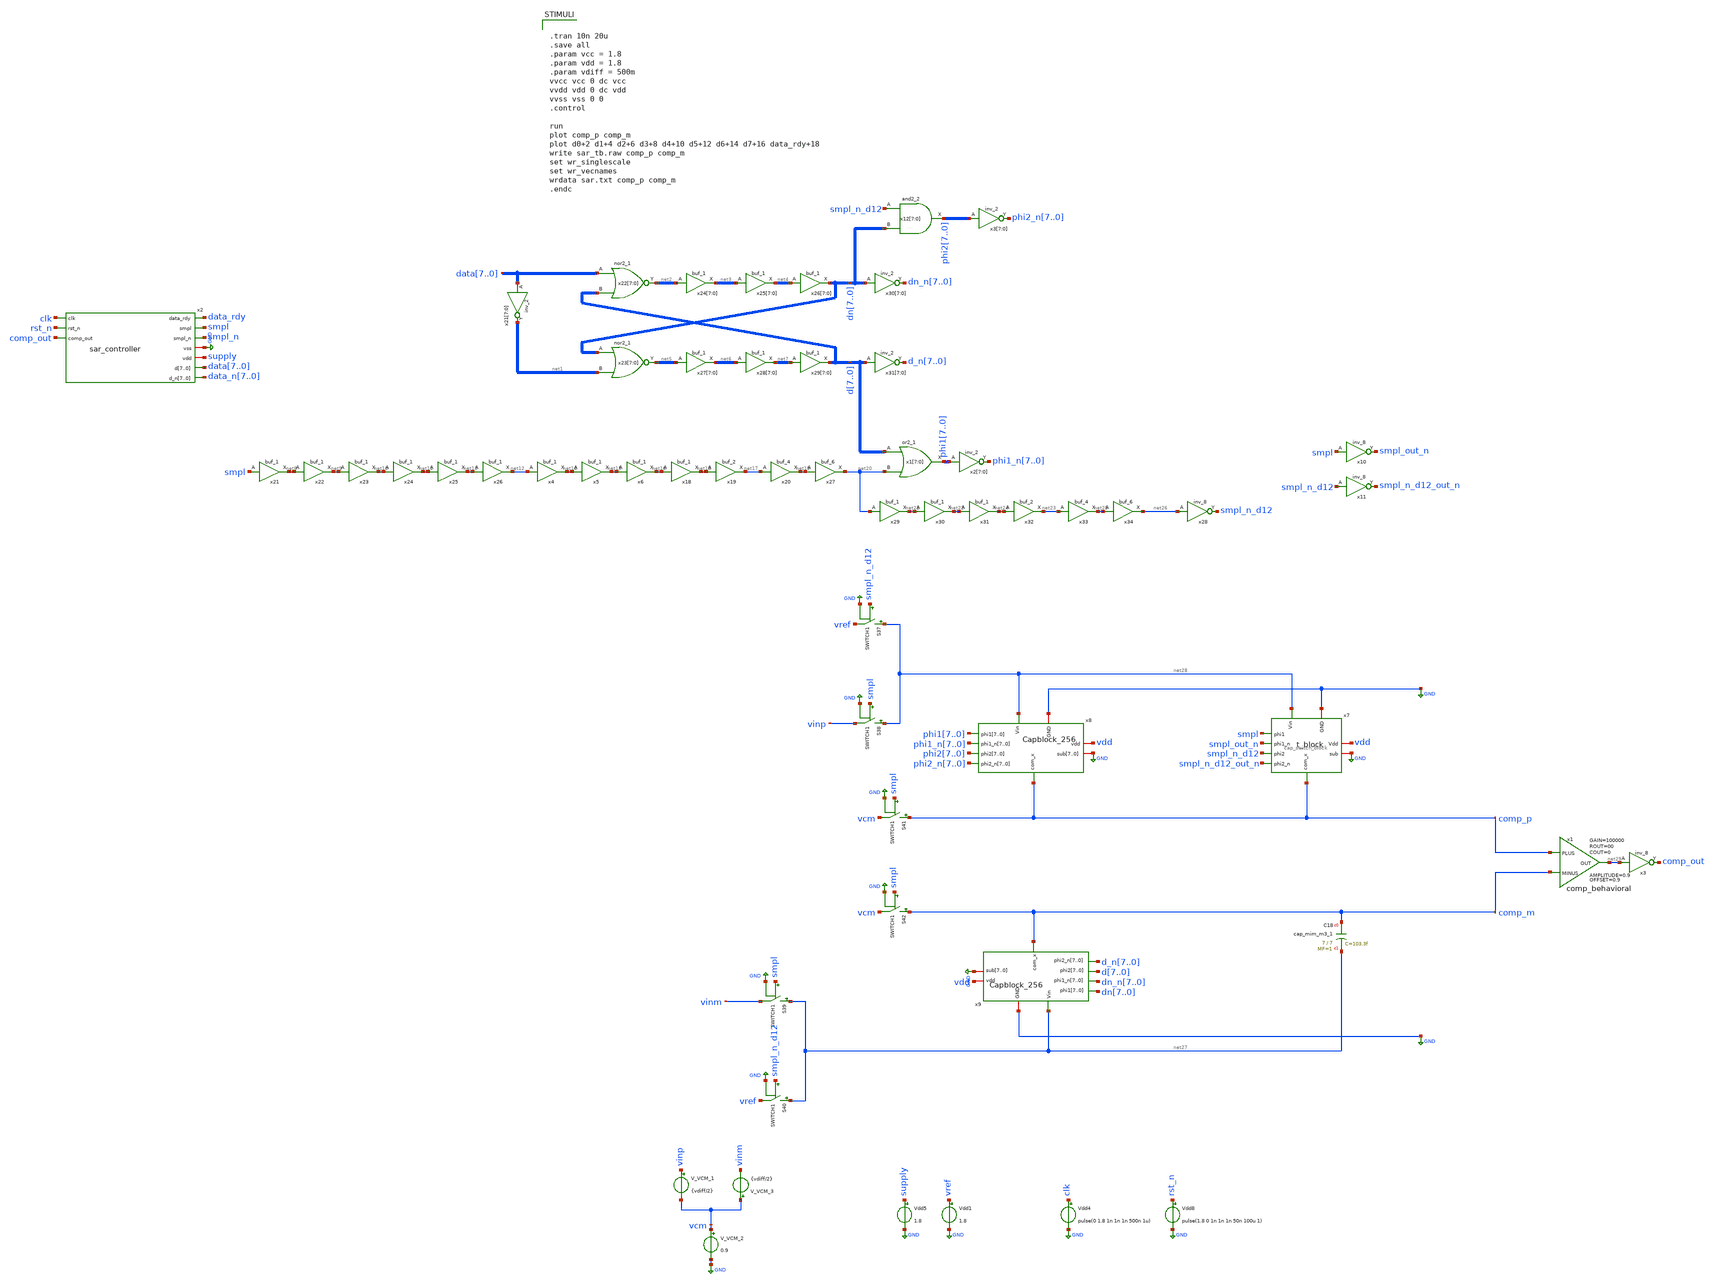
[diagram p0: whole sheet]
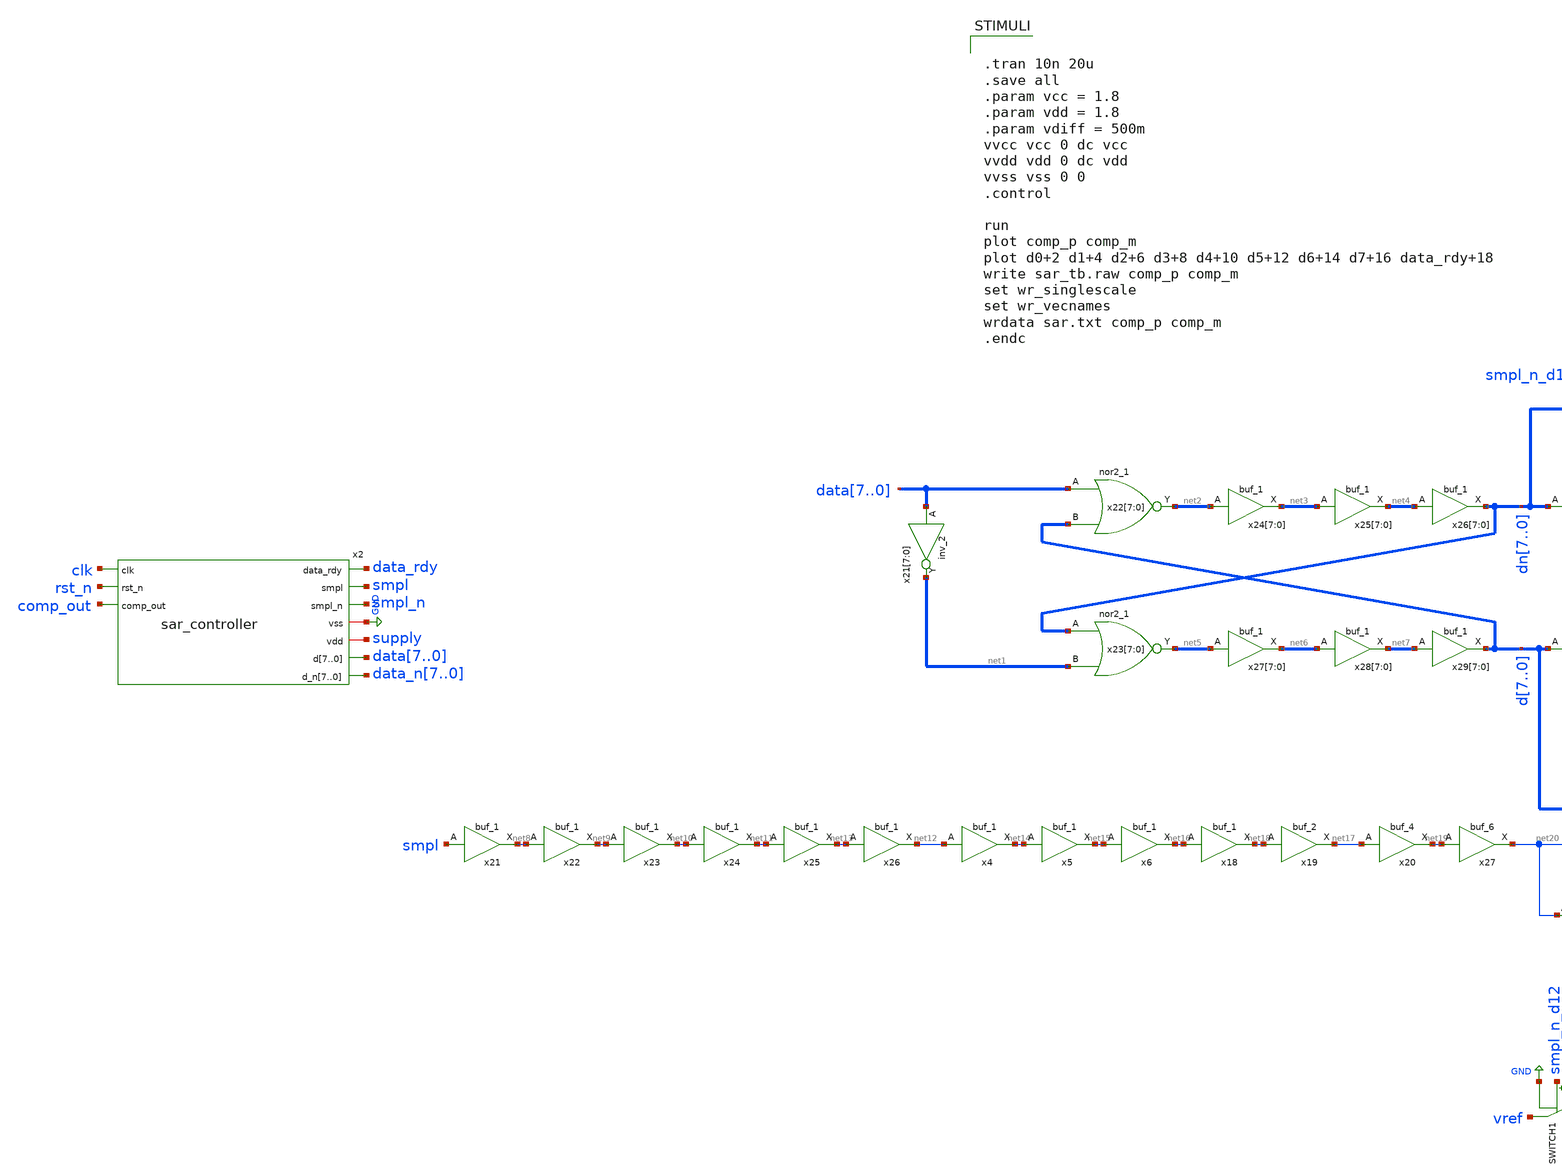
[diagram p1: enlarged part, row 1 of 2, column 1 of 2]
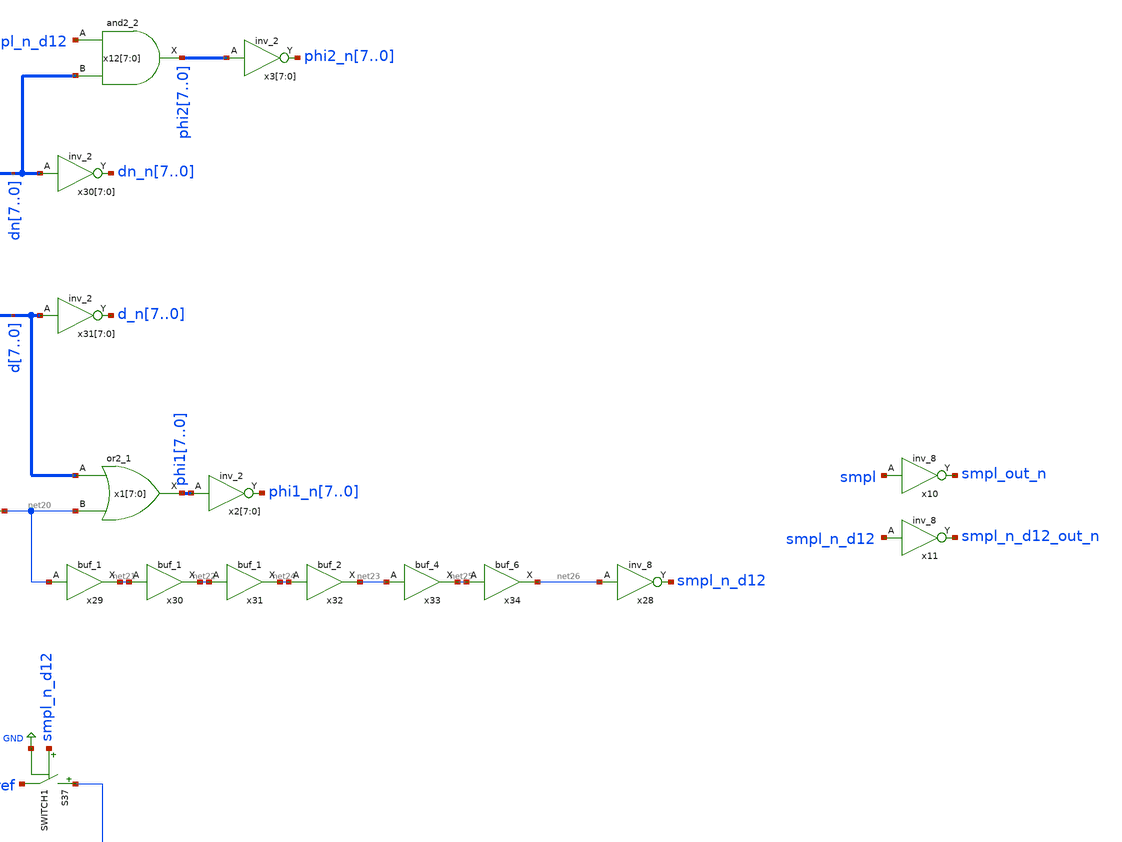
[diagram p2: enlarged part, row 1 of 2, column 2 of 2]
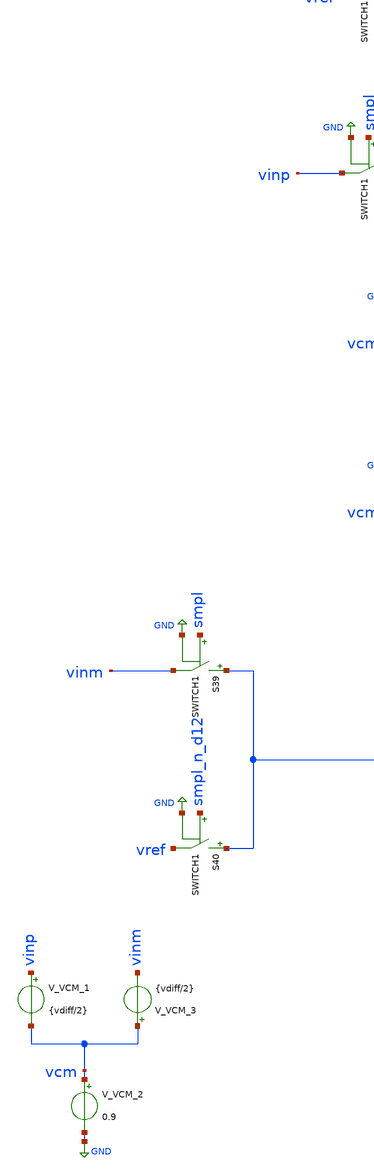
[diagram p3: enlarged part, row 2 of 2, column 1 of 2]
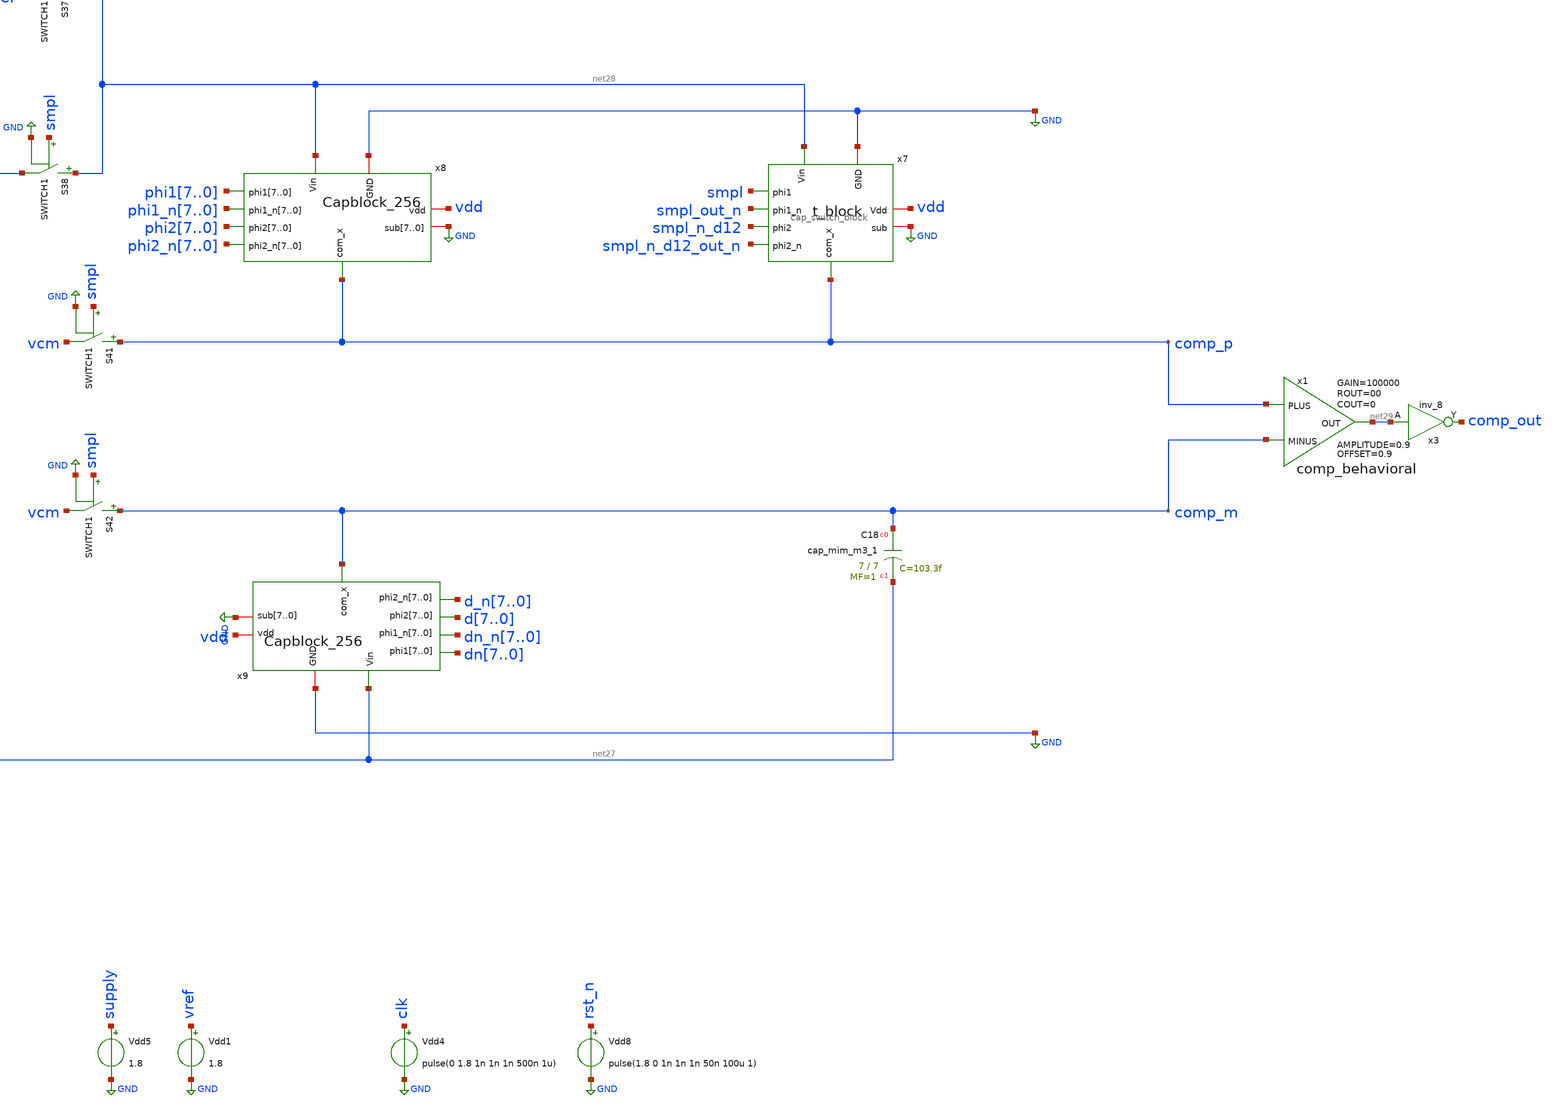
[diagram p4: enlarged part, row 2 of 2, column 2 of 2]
** sch_path: test/testbench/sar_tb_replace_cblock256.sch
.lib $::SKYWATER_MODELS/sky130.lib.spice tt
.include $::SKYWATER_STDCELLS/sky130_fd_sc_hd.spice

**.subckt sar_tb_replace_cblock256
Vdd8 rst_n GND pulse(1.8 0 1n 1n 1n 50n 100u 1)
Vdd4 clk GND pulse(0 1.8 1n 1n 1n 500n 1u)
Vdd1 vref GND 1.8
Vdd5 supply GND 1.8
V_VCM_2 vcm GND 0.9
V_VCM_1 vinp vcm {vdiff/2}
V_VCM_3 vcm vinm {vdiff/2}
x21[7] data7 vss vss vcc vcc net1[7] sky130_fd_sc_hd__inv_2
x21[6] data6 vss vss vcc vcc net1[6] sky130_fd_sc_hd__inv_2
x21[5] data5 vss vss vcc vcc net1[5] sky130_fd_sc_hd__inv_2
x21[4] data4 vss vss vcc vcc net1[4] sky130_fd_sc_hd__inv_2
x21[3] data3 vss vss vcc vcc net1[3] sky130_fd_sc_hd__inv_2
x21[2] data2 vss vss vcc vcc net1[2] sky130_fd_sc_hd__inv_2
x21[1] data1 vss vss vcc vcc net1[1] sky130_fd_sc_hd__inv_2
x21[0] data0 vss vss vcc vcc net1[0] sky130_fd_sc_hd__inv_2
x22[7] data7 d7 vss vss vdd vdd net2[7] sky130_fd_sc_hd__nor2_1
x22[6] data6 d6 vss vss vdd vdd net2[6] sky130_fd_sc_hd__nor2_1
x22[5] data5 d5 vss vss vdd vdd net2[5] sky130_fd_sc_hd__nor2_1
x22[4] data4 d4 vss vss vdd vdd net2[4] sky130_fd_sc_hd__nor2_1
x22[3] data3 d3 vss vss vdd vdd net2[3] sky130_fd_sc_hd__nor2_1
x22[2] data2 d2 vss vss vdd vdd net2[2] sky130_fd_sc_hd__nor2_1
x22[1] data1 d1 vss vss vdd vdd net2[1] sky130_fd_sc_hd__nor2_1
x22[0] data0 d0 vss vss vdd vdd net2[0] sky130_fd_sc_hd__nor2_1
x23[7] dn7 net1[7] vss vss vdd vdd net5[7] sky130_fd_sc_hd__nor2_1
x23[6] dn6 net1[6] vss vss vdd vdd net5[6] sky130_fd_sc_hd__nor2_1
x23[5] dn5 net1[5] vss vss vdd vdd net5[5] sky130_fd_sc_hd__nor2_1
x23[4] dn4 net1[4] vss vss vdd vdd net5[4] sky130_fd_sc_hd__nor2_1
x23[3] dn3 net1[3] vss vss vdd vdd net5[3] sky130_fd_sc_hd__nor2_1
x23[2] dn2 net1[2] vss vss vdd vdd net5[2] sky130_fd_sc_hd__nor2_1
x23[1] dn1 net1[1] vss vss vdd vdd net5[1] sky130_fd_sc_hd__nor2_1
x23[0] dn0 net1[0] vss vss vdd vdd net5[0] sky130_fd_sc_hd__nor2_1
x24[7] net2[7] vss vss vdd vdd net3[7] sky130_fd_sc_hd__buf_1
x24[6] net2[6] vss vss vdd vdd net3[6] sky130_fd_sc_hd__buf_1
x24[5] net2[5] vss vss vdd vdd net3[5] sky130_fd_sc_hd__buf_1
x24[4] net2[4] vss vss vdd vdd net3[4] sky130_fd_sc_hd__buf_1
x24[3] net2[3] vss vss vdd vdd net3[3] sky130_fd_sc_hd__buf_1
x24[2] net2[2] vss vss vdd vdd net3[2] sky130_fd_sc_hd__buf_1
x24[1] net2[1] vss vss vdd vdd net3[1] sky130_fd_sc_hd__buf_1
x24[0] net2[0] vss vss vdd vdd net3[0] sky130_fd_sc_hd__buf_1
x25[7] net3[7] vss vss vdd vdd net4[7] sky130_fd_sc_hd__buf_1
x25[6] net3[6] vss vss vdd vdd net4[6] sky130_fd_sc_hd__buf_1
x25[5] net3[5] vss vss vdd vdd net4[5] sky130_fd_sc_hd__buf_1
x25[4] net3[4] vss vss vdd vdd net4[4] sky130_fd_sc_hd__buf_1
x25[3] net3[3] vss vss vdd vdd net4[3] sky130_fd_sc_hd__buf_1
x25[2] net3[2] vss vss vdd vdd net4[2] sky130_fd_sc_hd__buf_1
x25[1] net3[1] vss vss vdd vdd net4[1] sky130_fd_sc_hd__buf_1
x25[0] net3[0] vss vss vdd vdd net4[0] sky130_fd_sc_hd__buf_1
x26[7] net4[7] vss vss vdd vdd dn7 sky130_fd_sc_hd__buf_1
x26[6] net4[6] vss vss vdd vdd dn6 sky130_fd_sc_hd__buf_1
x26[5] net4[5] vss vss vdd vdd dn5 sky130_fd_sc_hd__buf_1
x26[4] net4[4] vss vss vdd vdd dn4 sky130_fd_sc_hd__buf_1
x26[3] net4[3] vss vss vdd vdd dn3 sky130_fd_sc_hd__buf_1
x26[2] net4[2] vss vss vdd vdd dn2 sky130_fd_sc_hd__buf_1
x26[1] net4[1] vss vss vdd vdd dn1 sky130_fd_sc_hd__buf_1
x26[0] net4[0] vss vss vdd vdd dn0 sky130_fd_sc_hd__buf_1
x27[7] net5[7] vss vss vdd vdd net6[7] sky130_fd_sc_hd__buf_1
x27[6] net5[6] vss vss vdd vdd net6[6] sky130_fd_sc_hd__buf_1
x27[5] net5[5] vss vss vdd vdd net6[5] sky130_fd_sc_hd__buf_1
x27[4] net5[4] vss vss vdd vdd net6[4] sky130_fd_sc_hd__buf_1
x27[3] net5[3] vss vss vdd vdd net6[3] sky130_fd_sc_hd__buf_1
x27[2] net5[2] vss vss vdd vdd net6[2] sky130_fd_sc_hd__buf_1
x27[1] net5[1] vss vss vdd vdd net6[1] sky130_fd_sc_hd__buf_1
x27[0] net5[0] vss vss vdd vdd net6[0] sky130_fd_sc_hd__buf_1
x28[7] net6[7] vss vss vdd vdd net7[7] sky130_fd_sc_hd__buf_1
x28[6] net6[6] vss vss vdd vdd net7[6] sky130_fd_sc_hd__buf_1
x28[5] net6[5] vss vss vdd vdd net7[5] sky130_fd_sc_hd__buf_1
x28[4] net6[4] vss vss vdd vdd net7[4] sky130_fd_sc_hd__buf_1
x28[3] net6[3] vss vss vdd vdd net7[3] sky130_fd_sc_hd__buf_1
x28[2] net6[2] vss vss vdd vdd net7[2] sky130_fd_sc_hd__buf_1
x28[1] net6[1] vss vss vdd vdd net7[1] sky130_fd_sc_hd__buf_1
x28[0] net6[0] vss vss vdd vdd net7[0] sky130_fd_sc_hd__buf_1
x29[7] net7[7] vss vss vdd vdd d7 sky130_fd_sc_hd__buf_1
x29[6] net7[6] vss vss vdd vdd d6 sky130_fd_sc_hd__buf_1
x29[5] net7[5] vss vss vdd vdd d5 sky130_fd_sc_hd__buf_1
x29[4] net7[4] vss vss vdd vdd d4 sky130_fd_sc_hd__buf_1
x29[3] net7[3] vss vss vdd vdd d3 sky130_fd_sc_hd__buf_1
x29[2] net7[2] vss vss vdd vdd d2 sky130_fd_sc_hd__buf_1
x29[1] net7[1] vss vss vdd vdd d1 sky130_fd_sc_hd__buf_1
x29[0] net7[0] vss vss vdd vdd d0 sky130_fd_sc_hd__buf_1
x30[7] dn7 vss vss vcc vcc dn_n7 sky130_fd_sc_hd__inv_2
x30[6] dn6 vss vss vcc vcc dn_n6 sky130_fd_sc_hd__inv_2
x30[5] dn5 vss vss vcc vcc dn_n5 sky130_fd_sc_hd__inv_2
x30[4] dn4 vss vss vcc vcc dn_n4 sky130_fd_sc_hd__inv_2
x30[3] dn3 vss vss vcc vcc dn_n3 sky130_fd_sc_hd__inv_2
x30[2] dn2 vss vss vcc vcc dn_n2 sky130_fd_sc_hd__inv_2
x30[1] dn1 vss vss vcc vcc dn_n1 sky130_fd_sc_hd__inv_2
x30[0] dn0 vss vss vcc vcc dn_n0 sky130_fd_sc_hd__inv_2
x31[7] d7 vss vss vcc vcc d_n7 sky130_fd_sc_hd__inv_2
x31[6] d6 vss vss vcc vcc d_n6 sky130_fd_sc_hd__inv_2
x31[5] d5 vss vss vcc vcc d_n5 sky130_fd_sc_hd__inv_2
x31[4] d4 vss vss vcc vcc d_n4 sky130_fd_sc_hd__inv_2
x31[3] d3 vss vss vcc vcc d_n3 sky130_fd_sc_hd__inv_2
x31[2] d2 vss vss vcc vcc d_n2 sky130_fd_sc_hd__inv_2
x31[1] d1 vss vss vcc vcc d_n1 sky130_fd_sc_hd__inv_2
x31[0] d0 vss vss vcc vcc d_n0 sky130_fd_sc_hd__inv_2
x1[7] d7 net20 vss vss vcc vcc phi17 sky130_fd_sc_hd__or2_1
x1[6] d6 net20 vss vss vcc vcc phi16 sky130_fd_sc_hd__or2_1
x1[5] d5 net20 vss vss vcc vcc phi15 sky130_fd_sc_hd__or2_1
x1[4] d4 net20 vss vss vcc vcc phi14 sky130_fd_sc_hd__or2_1
x1[3] d3 net20 vss vss vcc vcc phi13 sky130_fd_sc_hd__or2_1
x1[2] d2 net20 vss vss vcc vcc phi12 sky130_fd_sc_hd__or2_1
x1[1] d1 net20 vss vss vcc vcc phi11 sky130_fd_sc_hd__or2_1
x1[0] d0 net20 vss vss vcc vcc phi10 sky130_fd_sc_hd__or2_1
x21 smpl vss vss vdd vdd net8 sky130_fd_sc_hd__buf_1
x22 net8 vss vss vdd vdd net9 sky130_fd_sc_hd__buf_1
x23 net9 vss vss vdd vdd net10 sky130_fd_sc_hd__buf_1
x24 net10 vss vss vdd vdd net11 sky130_fd_sc_hd__buf_1
x25 net11 vss vss vdd vdd net13 sky130_fd_sc_hd__buf_1
x26 net13 vss vss vdd vdd net12 sky130_fd_sc_hd__buf_1
x2[7] phi17 vss vss vcc vcc phi1_n7 sky130_fd_sc_hd__inv_2
x2[6] phi16 vss vss vcc vcc phi1_n6 sky130_fd_sc_hd__inv_2
x2[5] phi15 vss vss vcc vcc phi1_n5 sky130_fd_sc_hd__inv_2
x2[4] phi14 vss vss vcc vcc phi1_n4 sky130_fd_sc_hd__inv_2
x2[3] phi13 vss vss vcc vcc phi1_n3 sky130_fd_sc_hd__inv_2
x2[2] phi12 vss vss vcc vcc phi1_n2 sky130_fd_sc_hd__inv_2
x2[1] phi11 vss vss vcc vcc phi1_n1 sky130_fd_sc_hd__inv_2
x2[0] phi10 vss vss vcc vcc phi1_n0 sky130_fd_sc_hd__inv_2
x12[7] smpl_n_d12 dn7 vss vss vcc vcc phi27 sky130_fd_sc_hd__and2_2
x12[6] smpl_n_d12 dn6 vss vss vcc vcc phi26 sky130_fd_sc_hd__and2_2
x12[5] smpl_n_d12 dn5 vss vss vcc vcc phi25 sky130_fd_sc_hd__and2_2
x12[4] smpl_n_d12 dn4 vss vss vcc vcc phi24 sky130_fd_sc_hd__and2_2
x12[3] smpl_n_d12 dn3 vss vss vcc vcc phi23 sky130_fd_sc_hd__and2_2
x12[2] smpl_n_d12 dn2 vss vss vcc vcc phi22 sky130_fd_sc_hd__and2_2
x12[1] smpl_n_d12 dn1 vss vss vcc vcc phi21 sky130_fd_sc_hd__and2_2
x12[0] smpl_n_d12 dn0 vss vss vcc vcc phi20 sky130_fd_sc_hd__and2_2
x4 net12 vss vss vdd vdd net14 sky130_fd_sc_hd__buf_1
x5 net14 vss vss vdd vdd net15 sky130_fd_sc_hd__buf_1
x6 net15 vss vss vdd vdd net16 sky130_fd_sc_hd__buf_1
x18 net16 vss vss vdd vdd net18 sky130_fd_sc_hd__buf_1
x19 net18 vss vss vdd vdd net17 sky130_fd_sc_hd__buf_2
x20 net17 vss vss vdd vdd net19 sky130_fd_sc_hd__buf_4
x27 net19 vss vss vdd vdd net20 sky130_fd_sc_hd__buf_6
x28 net26 vss vss vcc vcc smpl_n_d12 sky130_fd_sc_hd__inv_8
x29 net20 vss vss vdd vdd net21 sky130_fd_sc_hd__buf_1
x30 net21 vss vss vdd vdd net22 sky130_fd_sc_hd__buf_1
x31 net22 vss vss vdd vdd net24 sky130_fd_sc_hd__buf_1
x32 net24 vss vss vdd vdd net23 sky130_fd_sc_hd__buf_2
x33 net23 vss vss vdd vdd net25 sky130_fd_sc_hd__buf_4
x34 net25 vss vss vdd vdd net26 sky130_fd_sc_hd__buf_6
x3[7] phi27 vss vss vcc vcc phi2_n7 sky130_fd_sc_hd__inv_2
x3[6] phi26 vss vss vcc vcc phi2_n6 sky130_fd_sc_hd__inv_2
x3[5] phi25 vss vss vcc vcc phi2_n5 sky130_fd_sc_hd__inv_2
x3[4] phi24 vss vss vcc vcc phi2_n4 sky130_fd_sc_hd__inv_2
x3[3] phi23 vss vss vcc vcc phi2_n3 sky130_fd_sc_hd__inv_2
x3[2] phi22 vss vss vcc vcc phi2_n2 sky130_fd_sc_hd__inv_2
x3[1] phi21 vss vss vcc vcc phi2_n1 sky130_fd_sc_hd__inv_2
x3[0] phi20 vss vss vcc vcc phi2_n0 sky130_fd_sc_hd__inv_2
x2 clk data_rdy smpl rst_n smpl_n comp_out GND supply data7 data6 data5 data4 data3 data2 data1
+ data0 data_n7 data_n6 data_n5 data_n4 data_n3 data_n2 data_n1 data_n0 sar_controller
XC18 comp_m net27 sky130_fd_pr__cap_mim_m3_1 W=7 L=7 MF=1 m=1
S37 net28 vref smpl_n_d12 GND SWITCH1
S41 comp_p vcm smpl GND SWITCH1
S42 comp_m vcm smpl GND SWITCH1
S38 net28 vinp smpl GND SWITCH1
x3 net29 vss vss vcc vcc comp_out sky130_fd_sc_hd__inv_8
x7 net28 GND GND vdd smpl smpl_n_d12 smpl_n_d12_out_n smpl_out_n comp_p cap_switch_block
x1 comp_p comp_m net29 comp_behavioral OFFSET=0.9 AMPLITUDE=0.9 GAIN=100000 ROUT=00 COUT=0
x8 GND phi17 phi16 phi15 phi14 phi13 phi12 phi11 phi10 phi1_n7 phi1_n6 phi1_n5 phi1_n4 phi1_n3
+ phi1_n2 phi1_n1 phi1_n0 phi27 phi26 phi25 phi24 phi23 phi22 phi21 phi20 phi2_n7 phi2_n6 phi2_n5 phi2_n4
+ phi2_n3 phi2_n2 phi2_n1 phi2_n0 comp_p net28 GND GND GND GND GND GND GND GND vdd capblock_256
x9 GND dn7 dn6 dn5 dn4 dn3 dn2 dn1 dn0 dn_n7 dn_n6 dn_n5 dn_n4 dn_n3 dn_n2 dn_n1 dn_n0 d7 d6 d5 d4
+ d3 d2 d1 d0 d_n7 d_n6 d_n5 d_n4 d_n3 d_n2 d_n1 d_n0 comp_m net27 GND GND GND GND GND GND GND GND vdd
+ capblock_256
S39 net27 vinm smpl GND SWITCH1
S40 net27 vref smpl_n_d12 GND SWITCH1
x10 smpl vss vss vcc vcc smpl_out_n sky130_fd_sc_hd__inv_8
x11 smpl_n_d12 vss vss vcc vcc smpl_n_d12_out_n sky130_fd_sc_hd__inv_8
**** begin user architecture code


.tran 10n 20u
.save all
.param vcc = 1.8
.param vdd = 1.8
.param vdiff = 500m
vvcc vcc 0 dc vcc
vvdd vdd 0 dc vdd
vvss vss 0 0
.control

run
plot comp_p comp_m
plot d0+2 d1+4 d2+6 d3+8 d4+10 d5+12 d6+14 d7+16 data_rdy+18
write sar_tb.raw comp_p comp_m
set wr_singlescale
set wr_vecnames
wrdata sar.txt comp_p comp_m
.endc



.model SWITCH1 sw vt=0.9 vh=0 ron=1 roff =100G

**** end user architecture code
**.ends

* expanding   symbol:  sar_controller.sym # of pins=10
** sym_path: test/design/sar_controller.sym
** sch_path: test/design/sar_controller.sch
.subckt sar_controller clk data_rdy smpl rst_n smpl_n comp_out vss vdd d7 d6 d5 d4 d3 d2 d1 d0 d_n7
+ d_n6 d_n5 d_n4 d_n3 d_n2 d_n1 d_n0
*.ipin rst_n
*.opin data_rdy
*.ipin clk
*.opin smpl
*.ipin comp_out
*.iopin vss
*.iopin vdd
*.opin d7,d6,d5,d4,d3,d2,d1,d0
*.opin d_n7,d_n6,d_n5,d_n4,d_n3,d_n2,d_n1,d_n0
*.opin smpl_n
x26 net2 net21 net22 net9 vss vss vdd vdd net1 net25 sky130_fd_sc_hd__dfbbp_1
x5 net19 net23 net20 vss vss vdd vdd cnv_7 net9 sky130_fd_sc_hd__dfrbp_1
* noconn #net33
x24 net19 net8 net20 vss vss vdd vdd net23 net24 sky130_fd_sc_hd__dfsbp_1
x6 net24 net20 vss vss vdd vdd net22 sky130_fd_sc_hd__and2_4
x1 net19 cnv_7 net20 vss vss vdd vdd cnv_6 net12 sky130_fd_sc_hd__dfrbp_1
x2 net19 cnv_6 net20 vss vss vdd vdd cnv_5 net13 sky130_fd_sc_hd__dfrbp_1
x3 net19 cnv_5 net20 vss vss vdd vdd cnv_4 net14 sky130_fd_sc_hd__dfrbp_1
x4 net19 cnv_4 net20 vss vss vdd vdd cnv_3 net15 sky130_fd_sc_hd__dfrbp_1
x7 net19 cnv_3 net20 vss vss vdd vdd cnv_2 net16 sky130_fd_sc_hd__dfrbp_1
x8 net19 cnv_2 net20 vss vss vdd vdd cnv_1 net17 sky130_fd_sc_hd__dfrbp_1
x9 net19 cnv_1 net20 vss vss vdd vdd cnv_0 net18 sky130_fd_sc_hd__dfrbp_1
x10 net19 cnv_0 net20 vss vss vdd vdd net8 net33 sky130_fd_sc_hd__dfrbp_1
x11 vss vss net22 vss vss vdd vdd net11 net34 sky130_fd_sc_hd__dfrbp_1
x12 net10 net21 net22 net12 vss vss vdd vdd net2 net26 sky130_fd_sc_hd__dfbbp_1
x13 net3 net21 net22 net13 vss vss vdd vdd net10 net27 sky130_fd_sc_hd__dfbbp_1
x14 net4 net21 net22 net14 vss vss vdd vdd net3 net28 sky130_fd_sc_hd__dfbbp_1
x15 net5 net21 net22 net15 vss vss vdd vdd net4 net29 sky130_fd_sc_hd__dfbbp_1
x16 net6 net21 net22 net16 vss vss vdd vdd net5 net30 sky130_fd_sc_hd__dfbbp_1
x17 net7 net21 net22 net17 vss vss vdd vdd net6 net31 sky130_fd_sc_hd__dfbbp_1
x18 net11 net21 net22 net18 vss vss vdd vdd net7 net32 sky130_fd_sc_hd__dfbbp_1
* noconn #net34
x19 net1 vss vss vdd vdd d7 sky130_fd_sc_hd__buf_2
x20 net25 vss vss vdd vdd d_n7 sky130_fd_sc_hd__buf_2
x21 net2 vss vss vdd vdd d6 sky130_fd_sc_hd__buf_2
x22 net26 vss vss vdd vdd d_n6 sky130_fd_sc_hd__buf_2
x23 net10 vss vss vdd vdd d5 sky130_fd_sc_hd__buf_2
x25 net27 vss vss vdd vdd d_n5 sky130_fd_sc_hd__buf_2
x27 net3 vss vss vdd vdd d4 sky130_fd_sc_hd__buf_2
x28 net28 vss vss vdd vdd d_n4 sky130_fd_sc_hd__buf_2
x29 net4 vss vss vdd vdd d3 sky130_fd_sc_hd__buf_2
x30 net29 vss vss vdd vdd d_n3 sky130_fd_sc_hd__buf_2
x31 net5 vss vss vdd vdd d2 sky130_fd_sc_hd__buf_2
x32 net30 vss vss vdd vdd d_n2 sky130_fd_sc_hd__buf_2
x33 net6 vss vss vdd vdd d1 sky130_fd_sc_hd__buf_2
x34 net31 vss vss vdd vdd d_n1 sky130_fd_sc_hd__buf_2
x35 net7 vss vss vdd vdd d0 sky130_fd_sc_hd__buf_2
x36 net32 vss vss vdd vdd d_n0 sky130_fd_sc_hd__buf_2
x37 net23 vss vss vdd vdd smpl sky130_fd_sc_hd__buf_2
x38 net24 vss vss vdd vdd smpl_n sky130_fd_sc_hd__buf_2
x39 net8 vss vss vdd vdd data_rdy sky130_fd_sc_hd__buf_2
x40 comp_out vss vss vdd vdd net21 sky130_fd_sc_hd__buf_4
x41 rst_n vss vss vdd vdd net20 sky130_fd_sc_hd__buf_4
x42 clk vss vss vdd vdd net19 sky130_fd_sc_hd__buf_4
.ends


* expanding   symbol:  cap_switch_block.sym # of pins=9
** sym_path: test/design/cap_switch_block.sym
** sch_path: test/design/cap_switch_block.sch
.subckt cap_switch_block Vin sub GND Vdd phi1 phi2 phi2_n phi1_n com_x
*.ipin Vin
*.opin com_x
*.ipin phi1
*.ipin phi1_n
*.iopin Vdd
*.iopin GND
*.iopin sub
*.ipin phi2
*.ipin phi2_n
XC9 com_x net1 sky130_fd_pr__cap_mim_m3_1 W=7 L=7 MF=1 m=1
x4 phi1 sub net1 Vin Vdd phi1_n tg_final
x1 phi2 sub net1 GND Vdd phi2_n tg_final
.ends


* expanding   symbol:  comp_behavioral.sym # of pins=3
** sym_path: Behavioral_model/comp_behavioral.sym
** sch_path: Behavioral_model/comp_behavioral.sch
.subckt comp_behavioral PLUS MINUS OUT  OFFSET=0.9 AMPLITUDE=0.9 GAIN=100000 ROUT=00 COUT=0
*.ipin PLUS
*.ipin MINUS
*.opin OUT
B1 IOUT 0 V = {OFFSET + AMPLITUDE/2*(tanh(V(IPLUS,IMINUS)*GAIN*2/AMPLITUDE))}
V1 IPLUS PLUS 3
V2 IMINUS MINUS 3
R1 OUT IOUT {ROUT} m=1
C3 OUT 0 {COUT} m=1
.ends


* expanding   symbol:  capblock_256.sym # of pins=9
** sym_path: test/design/capblock_256.sym
** sch_path: test/design/capblock_256.sch
.subckt capblock_256 GND phi17 phi16 phi15 phi14 phi13 phi12 phi11 phi10 phi1_n7 phi1_n6 phi1_n5
+ phi1_n4 phi1_n3 phi1_n2 phi1_n1 phi1_n0 phi27 phi26 phi25 phi24 phi23 phi22 phi21 phi20 phi2_n7 phi2_n6
+ phi2_n5 phi2_n4 phi2_n3 phi2_n2 phi2_n1 phi2_n0 com_x Vin sub7 sub6 sub5 sub4 sub3 sub2 sub1 sub0 vdd
*.ipin phi17,phi16,phi15,phi14,phi13,phi12,phi11,phi10
*.ipin phi1_n7,phi1_n6,phi1_n5,phi1_n4,phi1_n3,phi1_n2,phi1_n1,phi1_n0
*.iopin vdd
*.iopin GND
*.iopin sub7,sub6,sub5,sub4,sub3,sub2,sub1,sub0
*.ipin phi27,phi26,phi25,phi24,phi23,phi22,phi21,phi20
*.ipin phi2_n7,phi2_n6,phi2_n5,phi2_n4,phi2_n3,phi2_n2,phi2_n1,phi2_n0
*.ipin Vin
*.opin com_x
x8 Vin sub0 GND vdd phi10 phi20 phi2_n0 phi1_n0 com_x cap_switch_block
x9[1] Vin sub1 GND vdd phi11 phi21 phi2_n1 phi1_n1 com_x cap_switch_block
x9[0] Vin sub1 GND vdd phi11 phi21 phi2_n1 phi1_n1 com_x cap_switch_block
x4[3] Vin sub2 GND vdd phi12 phi22 phi2_n2 phi1_n2 com_x cap_switch_block
x4[2] Vin sub2 GND vdd phi12 phi22 phi2_n2 phi1_n2 com_x cap_switch_block
x4[1] Vin sub2 GND vdd phi12 phi22 phi2_n2 phi1_n2 com_x cap_switch_block
x4[0] Vin sub2 GND vdd phi12 phi22 phi2_n2 phi1_n2 com_x cap_switch_block
x5[7] Vin sub3 GND vdd phi13 phi23 phi2_n3 phi1_n3 com_x cap_switch_block
x5[6] Vin sub3 GND vdd phi13 phi23 phi2_n3 phi1_n3 com_x cap_switch_block
x5[5] Vin sub3 GND vdd phi13 phi23 phi2_n3 phi1_n3 com_x cap_switch_block
x5[4] Vin sub3 GND vdd phi13 phi23 phi2_n3 phi1_n3 com_x cap_switch_block
x5[3] Vin sub3 GND vdd phi13 phi23 phi2_n3 phi1_n3 com_x cap_switch_block
x5[2] Vin sub3 GND vdd phi13 phi23 phi2_n3 phi1_n3 com_x cap_switch_block
x5[1] Vin sub3 GND vdd phi13 phi23 phi2_n3 phi1_n3 com_x cap_switch_block
x5[0] Vin sub3 GND vdd phi13 phi23 phi2_n3 phi1_n3 com_x cap_switch_block
x6[15] Vin sub4 GND vdd phi14 phi24 phi2_n4 phi1_n4 com_x cap_switch_block
x6[14] Vin sub4 GND vdd phi14 phi24 phi2_n4 phi1_n4 com_x cap_switch_block
x6[13] Vin sub4 GND vdd phi14 phi24 phi2_n4 phi1_n4 com_x cap_switch_block
x6[12] Vin sub4 GND vdd phi14 phi24 phi2_n4 phi1_n4 com_x cap_switch_block
x6[11] Vin sub4 GND vdd phi14 phi24 phi2_n4 phi1_n4 com_x cap_switch_block
x6[10] Vin sub4 GND vdd phi14 phi24 phi2_n4 phi1_n4 com_x cap_switch_block
x6[9] Vin sub4 GND vdd phi14 phi24 phi2_n4 phi1_n4 com_x cap_switch_block
x6[8] Vin sub4 GND vdd phi14 phi24 phi2_n4 phi1_n4 com_x cap_switch_block
x6[7] Vin sub4 GND vdd phi14 phi24 phi2_n4 phi1_n4 com_x cap_switch_block
x6[6] Vin sub4 GND vdd phi14 phi24 phi2_n4 phi1_n4 com_x cap_switch_block
x6[5] Vin sub4 GND vdd phi14 phi24 phi2_n4 phi1_n4 com_x cap_switch_block
x6[4] Vin sub4 GND vdd phi14 phi24 phi2_n4 phi1_n4 com_x cap_switch_block
x6[3] Vin sub4 GND vdd phi14 phi24 phi2_n4 phi1_n4 com_x cap_switch_block
x6[2] Vin sub4 GND vdd phi14 phi24 phi2_n4 phi1_n4 com_x cap_switch_block
x6[1] Vin sub4 GND vdd phi14 phi24 phi2_n4 phi1_n4 com_x cap_switch_block
x6[0] Vin sub4 GND vdd phi14 phi24 phi2_n4 phi1_n4 com_x cap_switch_block
x7[31] Vin sub5 GND vdd phi15 phi25 phi2_n5 phi1_n5 com_x cap_switch_block
x7[30] Vin sub5 GND vdd phi15 phi25 phi2_n5 phi1_n5 com_x cap_switch_block
x7[29] Vin sub5 GND vdd phi15 phi25 phi2_n5 phi1_n5 com_x cap_switch_block
x7[28] Vin sub5 GND vdd phi15 phi25 phi2_n5 phi1_n5 com_x cap_switch_block
x7[27] Vin sub5 GND vdd phi15 phi25 phi2_n5 phi1_n5 com_x cap_switch_block
x7[26] Vin sub5 GND vdd phi15 phi25 phi2_n5 phi1_n5 com_x cap_switch_block
x7[25] Vin sub5 GND vdd phi15 phi25 phi2_n5 phi1_n5 com_x cap_switch_block
x7[24] Vin sub5 GND vdd phi15 phi25 phi2_n5 phi1_n5 com_x cap_switch_block
x7[23] Vin sub5 GND vdd phi15 phi25 phi2_n5 phi1_n5 com_x cap_switch_block
x7[22] Vin sub5 GND vdd phi15 phi25 phi2_n5 phi1_n5 com_x cap_switch_block
x7[21] Vin sub5 GND vdd phi15 phi25 phi2_n5 phi1_n5 com_x cap_switch_block
x7[20] Vin sub5 GND vdd phi15 phi25 phi2_n5 phi1_n5 com_x cap_switch_block
x7[19] Vin sub5 GND vdd phi15 phi25 phi2_n5 phi1_n5 com_x cap_switch_block
x7[18] Vin sub5 GND vdd phi15 phi25 phi2_n5 phi1_n5 com_x cap_switch_block
x7[17] Vin sub5 GND vdd phi15 phi25 phi2_n5 phi1_n5 com_x cap_switch_block
x7[16] Vin sub5 GND vdd phi15 phi25 phi2_n5 phi1_n5 com_x cap_switch_block
x7[15] Vin sub5 GND vdd phi15 phi25 phi2_n5 phi1_n5 com_x cap_switch_block
x7[14] Vin sub5 GND vdd phi15 phi25 phi2_n5 phi1_n5 com_x cap_switch_block
x7[13] Vin sub5 GND vdd phi15 phi25 phi2_n5 phi1_n5 com_x cap_switch_block
x7[12] Vin sub5 GND vdd phi15 phi25 phi2_n5 phi1_n5 com_x cap_switch_block
x7[11] Vin sub5 GND vdd phi15 phi25 phi2_n5 phi1_n5 com_x cap_switch_block
x7[10] Vin sub5 GND vdd phi15 phi25 phi2_n5 phi1_n5 com_x cap_switch_block
x7[9] Vin sub5 GND vdd phi15 phi25 phi2_n5 phi1_n5 com_x cap_switch_block
x7[8] Vin sub5 GND vdd phi15 phi25 phi2_n5 phi1_n5 com_x cap_switch_block
x7[7] Vin sub5 GND vdd phi15 phi25 phi2_n5 phi1_n5 com_x cap_switch_block
x7[6] Vin sub5 GND vdd phi15 phi25 phi2_n5 phi1_n5 com_x cap_switch_block
x7[5] Vin sub5 GND vdd phi15 phi25 phi2_n5 phi1_n5 com_x cap_switch_block
x7[4] Vin sub5 GND vdd phi15 phi25 phi2_n5 phi1_n5 com_x cap_switch_block
x7[3] Vin sub5 GND vdd phi15 phi25 phi2_n5 phi1_n5 com_x cap_switch_block
x7[2] Vin sub5 GND vdd phi15 phi25 phi2_n5 phi1_n5 com_x cap_switch_block
x7[1] Vin sub5 GND vdd phi15 phi25 phi2_n5 phi1_n5 com_x cap_switch_block
x7[0] Vin sub5 GND vdd phi15 phi25 phi2_n5 phi1_n5 com_x cap_switch_block
x8[63] Vin sub6 GND vdd phi16 phi26 phi2_n6 phi1_n6 com_x cap_switch_block
x8[62] Vin sub6 GND vdd phi16 phi26 phi2_n6 phi1_n6 com_x cap_switch_block
x8[61] Vin sub6 GND vdd phi16 phi26 phi2_n6 phi1_n6 com_x cap_switch_block
x8[60] Vin sub6 GND vdd phi16 phi26 phi2_n6 phi1_n6 com_x cap_switch_block
x8[59] Vin sub6 GND vdd phi16 phi26 phi2_n6 phi1_n6 com_x cap_switch_block
x8[58] Vin sub6 GND vdd phi16 phi26 phi2_n6 phi1_n6 com_x cap_switch_block
x8[57] Vin sub6 GND vdd phi16 phi26 phi2_n6 phi1_n6 com_x cap_switch_block
x8[56] Vin sub6 GND vdd phi16 phi26 phi2_n6 phi1_n6 com_x cap_switch_block
x8[55] Vin sub6 GND vdd phi16 phi26 phi2_n6 phi1_n6 com_x cap_switch_block
x8[54] Vin sub6 GND vdd phi16 phi26 phi2_n6 phi1_n6 com_x cap_switch_block
x8[53] Vin sub6 GND vdd phi16 phi26 phi2_n6 phi1_n6 com_x cap_switch_block
x8[52] Vin sub6 GND vdd phi16 phi26 phi2_n6 phi1_n6 com_x cap_switch_block
x8[51] Vin sub6 GND vdd phi16 phi26 phi2_n6 phi1_n6 com_x cap_switch_block
x8[50] Vin sub6 GND vdd phi16 phi26 phi2_n6 phi1_n6 com_x cap_switch_block
x8[49] Vin sub6 GND vdd phi16 phi26 phi2_n6 phi1_n6 com_x cap_switch_block
x8[48] Vin sub6 GND vdd phi16 phi26 phi2_n6 phi1_n6 com_x cap_switch_block
x8[47] Vin sub6 GND vdd phi16 phi26 phi2_n6 phi1_n6 com_x cap_switch_block
x8[46] Vin sub6 GND vdd phi16 phi26 phi2_n6 phi1_n6 com_x cap_switch_block
x8[45] Vin sub6 GND vdd phi16 phi26 phi2_n6 phi1_n6 com_x cap_switch_block
x8[44] Vin sub6 GND vdd phi16 phi26 phi2_n6 phi1_n6 com_x cap_switch_block
x8[43] Vin sub6 GND vdd phi16 phi26 phi2_n6 phi1_n6 com_x cap_switch_block
x8[42] Vin sub6 GND vdd phi16 phi26 phi2_n6 phi1_n6 com_x cap_switch_block
x8[41] Vin sub6 GND vdd phi16 phi26 phi2_n6 phi1_n6 com_x cap_switch_block
x8[40] Vin sub6 GND vdd phi16 phi26 phi2_n6 phi1_n6 com_x cap_switch_block
x8[39] Vin sub6 GND vdd phi16 phi26 phi2_n6 phi1_n6 com_x cap_switch_block
x8[38] Vin sub6 GND vdd phi16 phi26 phi2_n6 phi1_n6 com_x cap_switch_block
x8[37] Vin sub6 GND vdd phi16 phi26 phi2_n6 phi1_n6 com_x cap_switch_block
x8[36] Vin sub6 GND vdd phi16 phi26 phi2_n6 phi1_n6 com_x cap_switch_block
x8[35] Vin sub6 GND vdd phi16 phi26 phi2_n6 phi1_n6 com_x cap_switch_block
x8[34] Vin sub6 GND vdd phi16 phi26 phi2_n6 phi1_n6 com_x cap_switch_block
x8[33] Vin sub6 GND vdd phi16 phi26 phi2_n6 phi1_n6 com_x cap_switch_block
x8[32] Vin sub6 GND vdd phi16 phi26 phi2_n6 phi1_n6 com_x cap_switch_block
x8[31] Vin sub6 GND vdd phi16 phi26 phi2_n6 phi1_n6 com_x cap_switch_block
x8[30] Vin sub6 GND vdd phi16 phi26 phi2_n6 phi1_n6 com_x cap_switch_block
x8[29] Vin sub6 GND vdd phi16 phi26 phi2_n6 phi1_n6 com_x cap_switch_block
x8[28] Vin sub6 GND vdd phi16 phi26 phi2_n6 phi1_n6 com_x cap_switch_block
x8[27] Vin sub6 GND vdd phi16 phi26 phi2_n6 phi1_n6 com_x cap_switch_block
x8[26] Vin sub6 GND vdd phi16 phi26 phi2_n6 phi1_n6 com_x cap_switch_block
x8[25] Vin sub6 GND vdd phi16 phi26 phi2_n6 phi1_n6 com_x cap_switch_block
x8[24] Vin sub6 GND vdd phi16 phi26 phi2_n6 phi1_n6 com_x cap_switch_block
x8[23] Vin sub6 GND vdd phi16 phi26 phi2_n6 phi1_n6 com_x cap_switch_block
x8[22] Vin sub6 GND vdd phi16 phi26 phi2_n6 phi1_n6 com_x cap_switch_block
x8[21] Vin sub6 GND vdd phi16 phi26 phi2_n6 phi1_n6 com_x cap_switch_block
x8[20] Vin sub6 GND vdd phi16 phi26 phi2_n6 phi1_n6 com_x cap_switch_block
x8[19] Vin sub6 GND vdd phi16 phi26 phi2_n6 phi1_n6 com_x cap_switch_block
x8[18] Vin sub6 GND vdd phi16 phi26 phi2_n6 phi1_n6 com_x cap_switch_block
x8[17] Vin sub6 GND vdd phi16 phi26 phi2_n6 phi1_n6 com_x cap_switch_block
x8[16] Vin sub6 GND vdd phi16 phi26 phi2_n6 phi1_n6 com_x cap_switch_block
x8[15] Vin sub6 GND vdd phi16 phi26 phi2_n6 phi1_n6 com_x cap_switch_block
x8[14] Vin sub6 GND vdd phi16 phi26 phi2_n6 phi1_n6 com_x cap_switch_block
x8[13] Vin sub6 GND vdd phi16 phi26 phi2_n6 phi1_n6 com_x cap_switch_block
x8[12] Vin sub6 GND vdd phi16 phi26 phi2_n6 phi1_n6 com_x cap_switch_block
x8[11] Vin sub6 GND vdd phi16 phi26 phi2_n6 phi1_n6 com_x cap_switch_block
x8[10] Vin sub6 GND vdd phi16 phi26 phi2_n6 phi1_n6 com_x cap_switch_block
x8[9] Vin sub6 GND vdd phi16 phi26 phi2_n6 phi1_n6 com_x cap_switch_block
x8[8] Vin sub6 GND vdd phi16 phi26 phi2_n6 phi1_n6 com_x cap_switch_block
x8[7] Vin sub6 GND vdd phi16 phi26 phi2_n6 phi1_n6 com_x cap_switch_block
x8[6] Vin sub6 GND vdd phi16 phi26 phi2_n6 phi1_n6 com_x cap_switch_block
x8[5] Vin sub6 GND vdd phi16 phi26 phi2_n6 phi1_n6 com_x cap_switch_block
x8[4] Vin sub6 GND vdd phi16 phi26 phi2_n6 phi1_n6 com_x cap_switch_block
x8[3] Vin sub6 GND vdd phi16 phi26 phi2_n6 phi1_n6 com_x cap_switch_block
x8[2] Vin sub6 GND vdd phi16 phi26 phi2_n6 phi1_n6 com_x cap_switch_block
x8[1] Vin sub6 GND vdd phi16 phi26 phi2_n6 phi1_n6 com_x cap_switch_block
x8[0] Vin sub6 GND vdd phi16 phi26 phi2_n6 phi1_n6 com_x cap_switch_block
x10[128] Vin sub7 GND vdd phi17 phi27 phi2_n7 phi1_n7 com_x cap_switch_block
x10[127] Vin sub7 GND vdd phi17 phi27 phi2_n7 phi1_n7 com_x cap_switch_block
x10[126] Vin sub7 GND vdd phi17 phi27 phi2_n7 phi1_n7 com_x cap_switch_block
x10[125] Vin sub7 GND vdd phi17 phi27 phi2_n7 phi1_n7 com_x cap_switch_block
x10[124] Vin sub7 GND vdd phi17 phi27 phi2_n7 phi1_n7 com_x cap_switch_block
x10[123] Vin sub7 GND vdd phi17 phi27 phi2_n7 phi1_n7 com_x cap_switch_block
x10[122] Vin sub7 GND vdd phi17 phi27 phi2_n7 phi1_n7 com_x cap_switch_block
x10[121] Vin sub7 GND vdd phi17 phi27 phi2_n7 phi1_n7 com_x cap_switch_block
x10[120] Vin sub7 GND vdd phi17 phi27 phi2_n7 phi1_n7 com_x cap_switch_block
x10[119] Vin sub7 GND vdd phi17 phi27 phi2_n7 phi1_n7 com_x cap_switch_block
x10[118] Vin sub7 GND vdd phi17 phi27 phi2_n7 phi1_n7 com_x cap_switch_block
x10[117] Vin sub7 GND vdd phi17 phi27 phi2_n7 phi1_n7 com_x cap_switch_block
x10[116] Vin sub7 GND vdd phi17 phi27 phi2_n7 phi1_n7 com_x cap_switch_block
x10[115] Vin sub7 GND vdd phi17 phi27 phi2_n7 phi1_n7 com_x cap_switch_block
x10[114] Vin sub7 GND vdd phi17 phi27 phi2_n7 phi1_n7 com_x cap_switch_block
x10[113] Vin sub7 GND vdd phi17 phi27 phi2_n7 phi1_n7 com_x cap_switch_block
x10[112] Vin sub7 GND vdd phi17 phi27 phi2_n7 phi1_n7 com_x cap_switch_block
x10[111] Vin sub7 GND vdd phi17 phi27 phi2_n7 phi1_n7 com_x cap_switch_block
x10[110] Vin sub7 GND vdd phi17 phi27 phi2_n7 phi1_n7 com_x cap_switch_block
x10[109] Vin sub7 GND vdd phi17 phi27 phi2_n7 phi1_n7 com_x cap_switch_block
x10[108] Vin sub7 GND vdd phi17 phi27 phi2_n7 phi1_n7 com_x cap_switch_block
x10[107] Vin sub7 GND vdd phi17 phi27 phi2_n7 phi1_n7 com_x cap_switch_block
x10[106] Vin sub7 GND vdd phi17 phi27 phi2_n7 phi1_n7 com_x cap_switch_block
x10[105] Vin sub7 GND vdd phi17 phi27 phi2_n7 phi1_n7 com_x cap_switch_block
x10[104] Vin sub7 GND vdd phi17 phi27 phi2_n7 phi1_n7 com_x cap_switch_block
x10[103] Vin sub7 GND vdd phi17 phi27 phi2_n7 phi1_n7 com_x cap_switch_block
x10[102] Vin sub7 GND vdd phi17 phi27 phi2_n7 phi1_n7 com_x cap_switch_block
x10[101] Vin sub7 GND vdd phi17 phi27 phi2_n7 phi1_n7 com_x cap_switch_block
x10[100] Vin sub7 GND vdd phi17 phi27 phi2_n7 phi1_n7 com_x cap_switch_block
x10[99] Vin sub7 GND vdd phi17 phi27 phi2_n7 phi1_n7 com_x cap_switch_block
x10[98] Vin sub7 GND vdd phi17 phi27 phi2_n7 phi1_n7 com_x cap_switch_block
x10[97] Vin sub7 GND vdd phi17 phi27 phi2_n7 phi1_n7 com_x cap_switch_block
x10[96] Vin sub7 GND vdd phi17 phi27 phi2_n7 phi1_n7 com_x cap_switch_block
x10[95] Vin sub7 GND vdd phi17 phi27 phi2_n7 phi1_n7 com_x cap_switch_block
x10[94] Vin sub7 GND vdd phi17 phi27 phi2_n7 phi1_n7 com_x cap_switch_block
x10[93] Vin sub7 GND vdd phi17 phi27 phi2_n7 phi1_n7 com_x cap_switch_block
x10[92] Vin sub7 GND vdd phi17 phi27 phi2_n7 phi1_n7 com_x cap_switch_block
x10[91] Vin sub7 GND vdd phi17 phi27 phi2_n7 phi1_n7 com_x cap_switch_block
x10[90] Vin sub7 GND vdd phi17 phi27 phi2_n7 phi1_n7 com_x cap_switch_block
x10[89] Vin sub7 GND vdd phi17 phi27 phi2_n7 phi1_n7 com_x cap_switch_block
x10[88] Vin sub7 GND vdd phi17 phi27 phi2_n7 phi1_n7 com_x cap_switch_block
x10[87] Vin sub7 GND vdd phi17 phi27 phi2_n7 phi1_n7 com_x cap_switch_block
x10[86] Vin sub7 GND vdd phi17 phi27 phi2_n7 phi1_n7 com_x cap_switch_block
x10[85] Vin sub7 GND vdd phi17 phi27 phi2_n7 phi1_n7 com_x cap_switch_block
x10[84] Vin sub7 GND vdd phi17 phi27 phi2_n7 phi1_n7 com_x cap_switch_block
x10[83] Vin sub7 GND vdd phi17 phi27 phi2_n7 phi1_n7 com_x cap_switch_block
x10[82] Vin sub7 GND vdd phi17 phi27 phi2_n7 phi1_n7 com_x cap_switch_block
x10[81] Vin sub7 GND vdd phi17 phi27 phi2_n7 phi1_n7 com_x cap_switch_block
x10[80] Vin sub7 GND vdd phi17 phi27 phi2_n7 phi1_n7 com_x cap_switch_block
x10[79] Vin sub7 GND vdd phi17 phi27 phi2_n7 phi1_n7 com_x cap_switch_block
x10[78] Vin sub7 GND vdd phi17 phi27 phi2_n7 phi1_n7 com_x cap_switch_block
x10[77] Vin sub7 GND vdd phi17 phi27 phi2_n7 phi1_n7 com_x cap_switch_block
x10[76] Vin sub7 GND vdd phi17 phi27 phi2_n7 phi1_n7 com_x cap_switch_block
x10[75] Vin sub7 GND vdd phi17 phi27 phi2_n7 phi1_n7 com_x cap_switch_block
x10[74] Vin sub7 GND vdd phi17 phi27 phi2_n7 phi1_n7 com_x cap_switch_block
x10[73] Vin sub7 GND vdd phi17 phi27 phi2_n7 phi1_n7 com_x cap_switch_block
x10[72] Vin sub7 GND vdd phi17 phi27 phi2_n7 phi1_n7 com_x cap_switch_block
x10[71] Vin sub7 GND vdd phi17 phi27 phi2_n7 phi1_n7 com_x cap_switch_block
x10[70] Vin sub7 GND vdd phi17 phi27 phi2_n7 phi1_n7 com_x cap_switch_block
x10[69] Vin sub7 GND vdd phi17 phi27 phi2_n7 phi1_n7 com_x cap_switch_block
x10[68] Vin sub7 GND vdd phi17 phi27 phi2_n7 phi1_n7 com_x cap_switch_block
x10[67] Vin sub7 GND vdd phi17 phi27 phi2_n7 phi1_n7 com_x cap_switch_block
x10[66] Vin sub7 GND vdd phi17 phi27 phi2_n7 phi1_n7 com_x cap_switch_block
x10[65] Vin sub7 GND vdd phi17 phi27 phi2_n7 phi1_n7 com_x cap_switch_block
x10[64] Vin sub7 GND vdd phi17 phi27 phi2_n7 phi1_n7 com_x cap_switch_block
x10[63] Vin sub7 GND vdd phi17 phi27 phi2_n7 phi1_n7 com_x cap_switch_block
x10[62] Vin sub7 GND vdd phi17 phi27 phi2_n7 phi1_n7 com_x cap_switch_block
x10[61] Vin sub7 GND vdd phi17 phi27 phi2_n7 phi1_n7 com_x cap_switch_block
x10[60] Vin sub7 GND vdd phi17 phi27 phi2_n7 phi1_n7 com_x cap_switch_block
x10[59] Vin sub7 GND vdd phi17 phi27 phi2_n7 phi1_n7 com_x cap_switch_block
x10[58] Vin sub7 GND vdd phi17 phi27 phi2_n7 phi1_n7 com_x cap_switch_block
x10[57] Vin sub7 GND vdd phi17 phi27 phi2_n7 phi1_n7 com_x cap_switch_block
x10[56] Vin sub7 GND vdd phi17 phi27 phi2_n7 phi1_n7 com_x cap_switch_block
x10[55] Vin sub7 GND vdd phi17 phi27 phi2_n7 phi1_n7 com_x cap_switch_block
x10[54] Vin sub7 GND vdd phi17 phi27 phi2_n7 phi1_n7 com_x cap_switch_block
x10[53] Vin sub7 GND vdd phi17 phi27 phi2_n7 phi1_n7 com_x cap_switch_block
x10[52] Vin sub7 GND vdd phi17 phi27 phi2_n7 phi1_n7 com_x cap_switch_block
x10[51] Vin sub7 GND vdd phi17 phi27 phi2_n7 phi1_n7 com_x cap_switch_block
x10[50] Vin sub7 GND vdd phi17 phi27 phi2_n7 phi1_n7 com_x cap_switch_block
x10[49] Vin sub7 GND vdd phi17 phi27 phi2_n7 phi1_n7 com_x cap_switch_block
x10[48] Vin sub7 GND vdd phi17 phi27 phi2_n7 phi1_n7 com_x cap_switch_block
x10[47] Vin sub7 GND vdd phi17 phi27 phi2_n7 phi1_n7 com_x cap_switch_block
x10[46] Vin sub7 GND vdd phi17 phi27 phi2_n7 phi1_n7 com_x cap_switch_block
x10[45] Vin sub7 GND vdd phi17 phi27 phi2_n7 phi1_n7 com_x cap_switch_block
x10[44] Vin sub7 GND vdd phi17 phi27 phi2_n7 phi1_n7 com_x cap_switch_block
x10[43] Vin sub7 GND vdd phi17 phi27 phi2_n7 phi1_n7 com_x cap_switch_block
x10[42] Vin sub7 GND vdd phi17 phi27 phi2_n7 phi1_n7 com_x cap_switch_block
x10[41] Vin sub7 GND vdd phi17 phi27 phi2_n7 phi1_n7 com_x cap_switch_block
x10[40] Vin sub7 GND vdd phi17 phi27 phi2_n7 phi1_n7 com_x cap_switch_block
x10[39] Vin sub7 GND vdd phi17 phi27 phi2_n7 phi1_n7 com_x cap_switch_block
x10[38] Vin sub7 GND vdd phi17 phi27 phi2_n7 phi1_n7 com_x cap_switch_block
x10[37] Vin sub7 GND vdd phi17 phi27 phi2_n7 phi1_n7 com_x cap_switch_block
x10[36] Vin sub7 GND vdd phi17 phi27 phi2_n7 phi1_n7 com_x cap_switch_block
x10[35] Vin sub7 GND vdd phi17 phi27 phi2_n7 phi1_n7 com_x cap_switch_block
x10[34] Vin sub7 GND vdd phi17 phi27 phi2_n7 phi1_n7 com_x cap_switch_block
x10[33] Vin sub7 GND vdd phi17 phi27 phi2_n7 phi1_n7 com_x cap_switch_block
x10[32] Vin sub7 GND vdd phi17 phi27 phi2_n7 phi1_n7 com_x cap_switch_block
x10[31] Vin sub7 GND vdd phi17 phi27 phi2_n7 phi1_n7 com_x cap_switch_block
x10[30] Vin sub7 GND vdd phi17 phi27 phi2_n7 phi1_n7 com_x cap_switch_block
x10[29] Vin sub7 GND vdd phi17 phi27 phi2_n7 phi1_n7 com_x cap_switch_block
x10[28] Vin sub7 GND vdd phi17 phi27 phi2_n7 phi1_n7 com_x cap_switch_block
x10[27] Vin sub7 GND vdd phi17 phi27 phi2_n7 phi1_n7 com_x cap_switch_block
x10[26] Vin sub7 GND vdd phi17 phi27 phi2_n7 phi1_n7 com_x cap_switch_block
x10[25] Vin sub7 GND vdd phi17 phi27 phi2_n7 phi1_n7 com_x cap_switch_block
x10[24] Vin sub7 GND vdd phi17 phi27 phi2_n7 phi1_n7 com_x cap_switch_block
x10[23] Vin sub7 GND vdd phi17 phi27 phi2_n7 phi1_n7 com_x cap_switch_block
x10[22] Vin sub7 GND vdd phi17 phi27 phi2_n7 phi1_n7 com_x cap_switch_block
x10[21] Vin sub7 GND vdd phi17 phi27 phi2_n7 phi1_n7 com_x cap_switch_block
x10[20] Vin sub7 GND vdd phi17 phi27 phi2_n7 phi1_n7 com_x cap_switch_block
x10[19] Vin sub7 GND vdd phi17 phi27 phi2_n7 phi1_n7 com_x cap_switch_block
x10[18] Vin sub7 GND vdd phi17 phi27 phi2_n7 phi1_n7 com_x cap_switch_block
x10[17] Vin sub7 GND vdd phi17 phi27 phi2_n7 phi1_n7 com_x cap_switch_block
x10[16] Vin sub7 GND vdd phi17 phi27 phi2_n7 phi1_n7 com_x cap_switch_block
x10[15] Vin sub7 GND vdd phi17 phi27 phi2_n7 phi1_n7 com_x cap_switch_block
x10[14] Vin sub7 GND vdd phi17 phi27 phi2_n7 phi1_n7 com_x cap_switch_block
x10[13] Vin sub7 GND vdd phi17 phi27 phi2_n7 phi1_n7 com_x cap_switch_block
x10[12] Vin sub7 GND vdd phi17 phi27 phi2_n7 phi1_n7 com_x cap_switch_block
x10[11] Vin sub7 GND vdd phi17 phi27 phi2_n7 phi1_n7 com_x cap_switch_block
x10[10] Vin sub7 GND vdd phi17 phi27 phi2_n7 phi1_n7 com_x cap_switch_block
x10[9] Vin sub7 GND vdd phi17 phi27 phi2_n7 phi1_n7 com_x cap_switch_block
x10[8] Vin sub7 GND vdd phi17 phi27 phi2_n7 phi1_n7 com_x cap_switch_block
x10[7] Vin sub7 GND vdd phi17 phi27 phi2_n7 phi1_n7 com_x cap_switch_block
x10[6] Vin sub7 GND vdd phi17 phi27 phi2_n7 phi1_n7 com_x cap_switch_block
x10[5] Vin sub7 GND vdd phi17 phi27 phi2_n7 phi1_n7 com_x cap_switch_block
x10[4] Vin sub7 GND vdd phi17 phi27 phi2_n7 phi1_n7 com_x cap_switch_block
x10[3] Vin sub7 GND vdd phi17 phi27 phi2_n7 phi1_n7 com_x cap_switch_block
x10[2] Vin sub7 GND vdd phi17 phi27 phi2_n7 phi1_n7 com_x cap_switch_block
x10[1] Vin sub7 GND vdd phi17 phi27 phi2_n7 phi1_n7 com_x cap_switch_block
x10[0] Vin sub7 GND vdd phi17 phi27 phi2_n7 phi1_n7 com_x cap_switch_block
.ends


* expanding   symbol:  final/tg_final.sym # of pins=6
** sym_path: top/test/design/tg_final.sym
** sch_path: top/test/design/tg_final.sch
.subckt tg_final clk sub vout vin vdd clk_b
*.ipin clk
*.ipin vin
*.opin vout
*.ipin vdd
*.ipin sub
*.ipin clk_b
XM2 vout clk vin sub sky130_fd_pr__nfet_01v8 L=0.15 W=1 nf=1 ad='int((nf+1)/2) * W/nf * 0.29' as='int((nf+2)/2) * W/nf * 0.29'
+ pd='2*int((nf+1)/2) * (W/nf + 0.29)' ps='2*int((nf+2)/2) * (W/nf + 0.29)' nrd='0.29 / W' nrs='0.29 / W'
+ sa=0 sb=0 sd=0 mult=1 m=1
XM1 vout clk_b vin vdd sky130_fd_pr__pfet_01v8 L=0.15 W=1 nf=1 ad='int((nf+1)/2) * W/nf * 0.29' as='int((nf+2)/2) * W/nf * 0.29'
+ pd='2*int((nf+1)/2) * (W/nf + 0.29)' ps='2*int((nf+2)/2) * (W/nf + 0.29)' nrd='0.29 / W' nrs='0.29 / W'
+ sa=0 sb=0 sd=0 mult=1 m=1
.ends

.GLOBAL GND
.end
